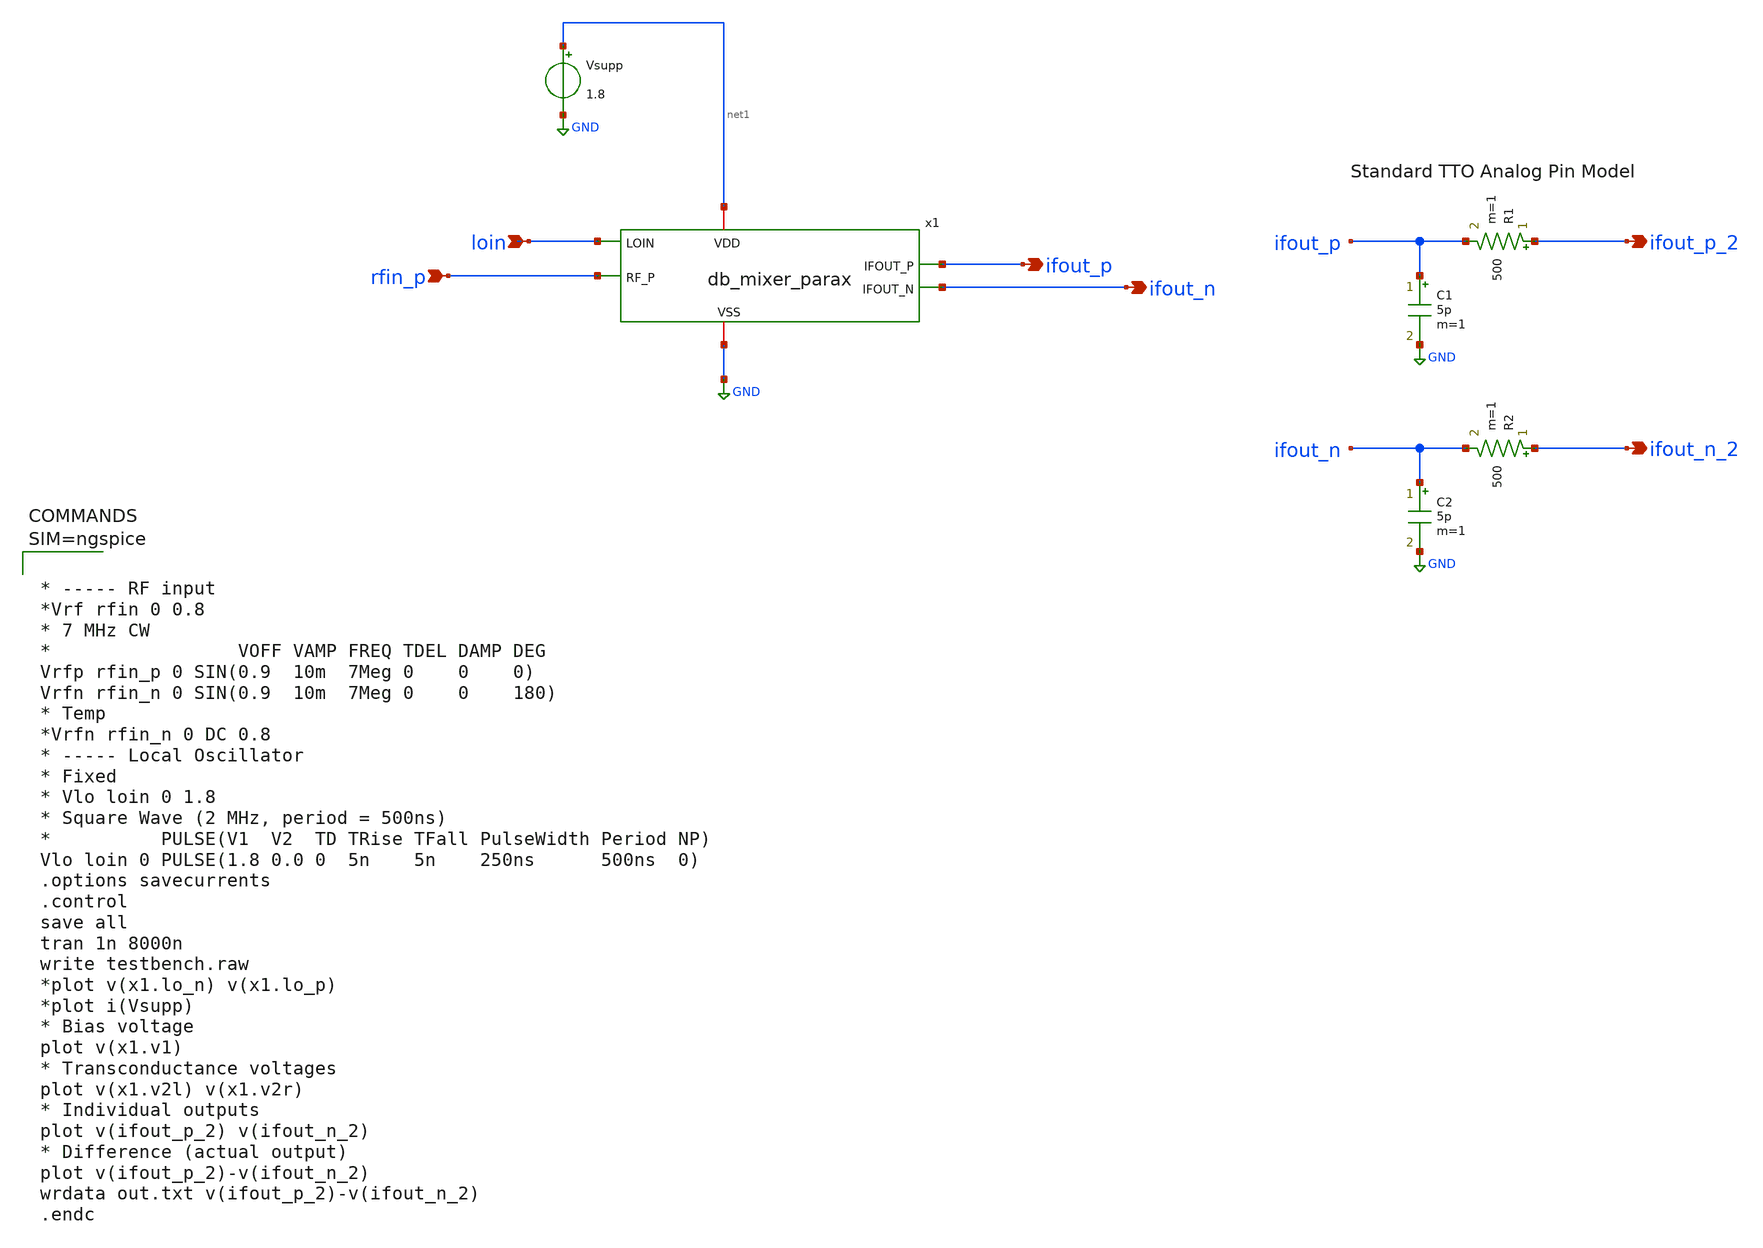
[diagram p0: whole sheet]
** sch_path: xschem/testbench_db2.sch
**.subckt testbench_db2 loin rfin_p ifout_p ifout_n ifout_p_2 ifout_n_2
*.ipin loin
*.ipin rfin_p
*.opin ifout_p
*.opin ifout_n
*.opin ifout_p_2
*.opin ifout_n_2
C1 ifout_p GND 5p m=1
R1 ifout_p_2 ifout_p 500 m=1
C2 ifout_n GND 5p m=1
R2 ifout_n_2 ifout_n 500 m=1
Vsupp net1 GND 1.8
x1 net1 GND loin ifout_n ifout_p rfin_p db_mixer_parax
**** begin user architecture code

** opencircuitdesign pdks install
.lib $::SKYWATER_MODELS/sky130.lib.spice tt
.include $::SKYWATER_STDCELLS/sky130_fd_sc_hd.spice





* ----- RF input
*Vrf rfin 0 0.8
* 7 MHz CW
*                 VOFF VAMP FREQ TDEL DAMP DEG
Vrfp rfin_p 0 SIN(0.9  10m  7Meg 0    0    0)
Vrfn rfin_n 0 SIN(0.9  10m  7Meg 0    0    180)
* Temp
*Vrfn rfin_n 0 DC 0.8
* ----- Local Oscillator
* Fixed
* Vlo loin 0 1.8
* Square Wave (2 MHz, period = 500ns)
*          PULSE(V1  V2  TD TRise TFall PulseWidth Period NP)
Vlo loin 0 PULSE(1.8 0.0 0  5n    5n    250ns      500ns  0)
.options savecurrents
.control
save all
tran 1n 8000n
write testbench.raw
*plot v(x1.lo_n) v(x1.lo_p)
*plot i(Vsupp)
* Bias voltage
plot v(x1.v1)
* Transconductance voltages
plot v(x1.v2l) v(x1.v2r)
* Individual outputs
plot v(ifout_p_2) v(ifout_n_2)
* Difference (actual output)
plot v(ifout_p_2)-v(ifout_n_2)
wrdata out.txt v(ifout_p_2)-v(ifout_n_2)
.endc



**** end user architecture code
**.ends

* expanding   symbol:  db_mixer_parax.sym # of pins=6
** sym_path: xschem/db_mixer.sym
.include [file normalize ../mag/db_mixer.sim.spice]
.GLOBAL GND
.end
